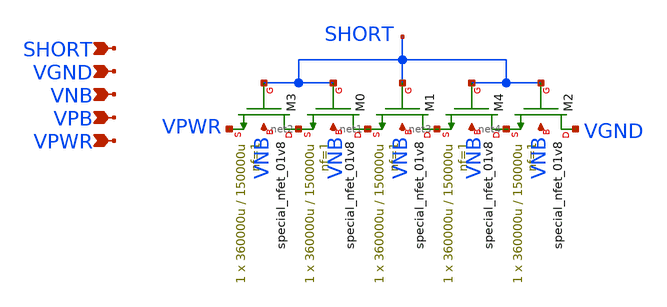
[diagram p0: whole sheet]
** sch_path: schematics/lpflow_bleeder/sky130_fd_sc_hd__lpflow_bleeder_1.sch
**.subckt sky130_fd_sc_hd__lpflow_bleeder_1 SHORT VGND VNB VPB VPWR
*.ipin SHORT
*.ipin VGND
*.ipin VNB
*.ipin VPB
*.ipin VPWR
XM0 net1 SHORT net2 VNB sky130_fd_pr__special_nfet_01v8 L=150000u W=360000u nf=1 ad='int((1 + 1)/2) * 360000u / 1 * 0.29'
+ as='int((1 + 2)/2) * 360000u / 1 * 0.29' pd='2*int((1 + 1)/2) * (360000u / 1 + 0.29)' ps='2*int((1 + 2)/2) * (360000u / 1 + 0.29)'
+ nrd='0.29 / 360000u ' nrs='0.29 / 360000u ' sa=0 sb=0 sd=0 mult=1 m=1
XM1 net3 SHORT net1 VNB sky130_fd_pr__special_nfet_01v8 L=150000u W=360000u nf=1 ad='int((1 + 1)/2) * 360000u / 1 * 0.29'
+ as='int((1 + 2)/2) * 360000u / 1 * 0.29' pd='2*int((1 + 1)/2) * (360000u / 1 + 0.29)' ps='2*int((1 + 2)/2) * (360000u / 1 + 0.29)'
+ nrd='0.29 / 360000u ' nrs='0.29 / 360000u ' sa=0 sb=0 sd=0 mult=1 m=1
XM2 VGND SHORT net4 VNB sky130_fd_pr__special_nfet_01v8 L=150000u W=360000u nf=1 ad='int((1 + 1)/2) * 360000u / 1 * 0.29'
+ as='int((1 + 2)/2) * 360000u / 1 * 0.29' pd='2*int((1 + 1)/2) * (360000u / 1 + 0.29)' ps='2*int((1 + 2)/2) * (360000u / 1 + 0.29)'
+ nrd='0.29 / 360000u ' nrs='0.29 / 360000u ' sa=0 sb=0 sd=0 mult=1 m=1
XM3 net2 SHORT VPWR VNB sky130_fd_pr__special_nfet_01v8 L=150000u W=360000u nf=1 ad='int((1 + 1)/2) * 360000u / 1 * 0.29'
+ as='int((1 + 2)/2) * 360000u / 1 * 0.29' pd='2*int((1 + 1)/2) * (360000u / 1 + 0.29)' ps='2*int((1 + 2)/2) * (360000u / 1 + 0.29)'
+ nrd='0.29 / 360000u ' nrs='0.29 / 360000u ' sa=0 sb=0 sd=0 mult=1 m=1
XM4 net4 SHORT net3 VNB sky130_fd_pr__special_nfet_01v8 L=150000u W=360000u nf=1 ad='int((1 + 1)/2) * 360000u / 1 * 0.29'
+ as='int((1 + 2)/2) * 360000u / 1 * 0.29' pd='2*int((1 + 1)/2) * (360000u / 1 + 0.29)' ps='2*int((1 + 2)/2) * (360000u / 1 + 0.29)'
+ nrd='0.29 / 360000u ' nrs='0.29 / 360000u ' sa=0 sb=0 sd=0 mult=1 m=1
**.ends
.end
